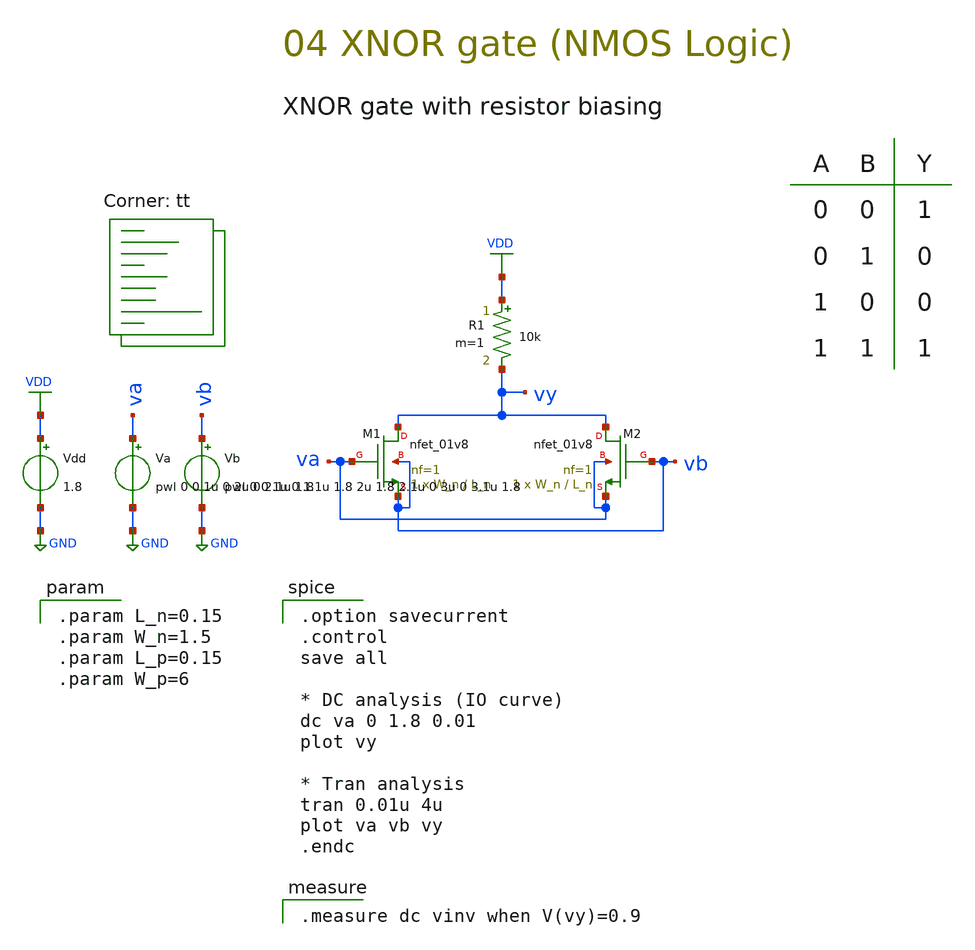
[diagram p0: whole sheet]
** sch_path: 04-a_XNOR_R.sch
**.subckt 04-a_XNOR_R
Vdd VDD GND 1.8
XM1 vy va vb vb sky130_fd_pr__nfet_01v8 L=L_n W=W_n nf=1 ad='int((1 + 1)/2) * W_n / 1 * 0.29' as='int((1 + 2)/2) * W_n / 1 * 0.29'
+ pd='2*int((1 + 1)/2) * (W_n / 1 + 0.29)' ps='2*int((1 + 2)/2) * (W_n / 1 + 0.29)' nrd='0.29 / W_n ' nrs='0.29 / W_n '
+ sa=0 sb=0 sd=0 mult=1 m=1
XM2 vy vb va va sky130_fd_pr__nfet_01v8 L=L_n W=W_n nf=1 ad='int((1 + 1)/2) * W_n / 1 * 0.29' as='int((1 + 2)/2) * W_n / 1 * 0.29'
+ pd='2*int((1 + 1)/2) * (W_n / 1 + 0.29)' ps='2*int((1 + 2)/2) * (W_n / 1 + 0.29)' nrd='0.29 / W_n ' nrs='0.29 / W_n '
+ sa=0 sb=0 sd=0 mult=1 m=1
Va va GND pwl 0 0 1u 0 2u 0 2.1u 1.8
Vb vb GND pwl 0 0 1u 0 1.1u 1.8 2u 1.8 2.1u 0 3u 0 3.1u 1.8
R1 VDD vy 10k m=1
**** begin user architecture code
.lib $::SKYWATER_MODELS/sky130.lib.spice tt

.option savecurrent
.control
save all

* DC analysis (IO curve)
dc va 0 1.8 0.01
plot vy

* Tran analysis
tran 0.01u 4u
plot va vb vy
.endc


.measure dc vinv when V(vy)=0.9


.param L_n=0.15
.param W_n=1.5
.param L_p=0.15
.param W_p=6

**** end user architecture code
**.ends
.GLOBAL GND
.GLOBAL VDD
.end
